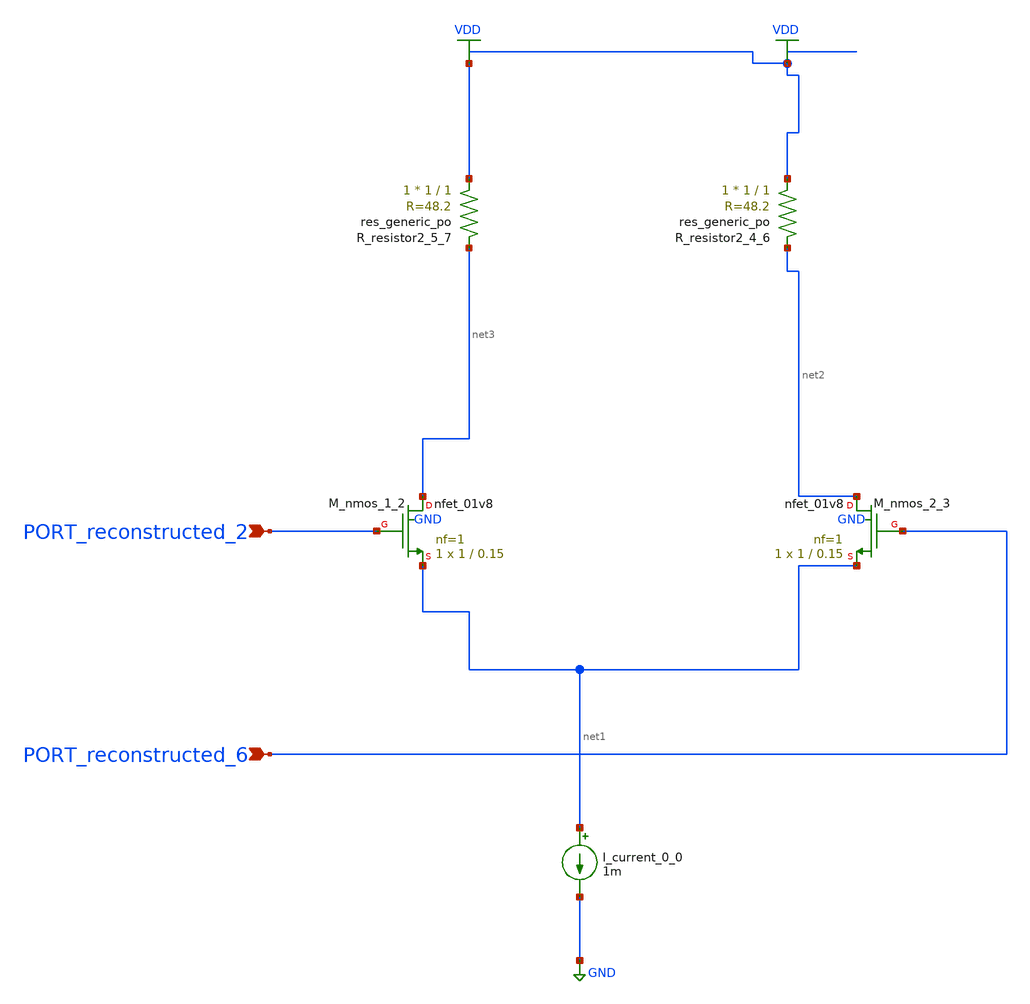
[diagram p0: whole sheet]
** sch_path: schematics/AMSNet/194.sch
**.subckt 194 PORT_reconstructed_6 PORT_reconstructed_2
*.ipin PORT_reconstructed_6
*.ipin PORT_reconstructed_2
I_current_0_0 net1 GND 1m
XM_nmos_1_2 net3 PORT_reconstructed_2 net1 GND sky130_fd_pr__nfet_01v8 L=0.15 W=1 nf=1 ad='int((1 + 1)/2) * 1 / 1 * 0.29'
+ as='int((1 + 2)/2) * 1 / 1 * 0.29' pd='2*int((1 + 1)/2) * (1 / 1 + 0.29)' ps='2*int((1 + 2)/2) * (1 / 1 + 0.29)'
+ nrd='0.29 / 1 ' nrs='0.29 / 1 ' sa=0 sb=0 sd=0 mult=1 m=1
XM_nmos_2_3 net2 PORT_reconstructed_6 net1 GND sky130_fd_pr__nfet_01v8 L=0.15 W=1 nf=1 ad='int((1 + 1)/2) * 1 / 1 * 0.29'
+ as='int((1 + 2)/2) * 1 / 1 * 0.29' pd='2*int((1 + 1)/2) * (1 / 1 + 0.29)' ps='2*int((1 + 2)/2) * (1 / 1 + 0.29)'
+ nrd='0.29 / 1 ' nrs='0.29 / 1 ' sa=0 sb=0 sd=0 mult=1 m=1
XR_resistor2_4_6 VDD net2 sky130_fd_pr__res_generic_po W=1 L=1 m=1
XR_resistor2_5_7 VDD net3 sky130_fd_pr__res_generic_po W=1 L=1 m=1
**.ends
.GLOBAL GND
.GLOBAL VDD
.end
